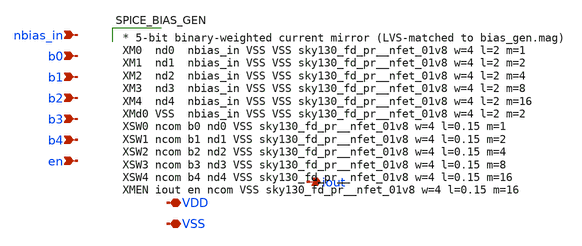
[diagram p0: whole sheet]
** sch_path: bvm_analog_tapeout/analog/bias_gen/xschem/bias_gen.sch
**.subckt bias_gen nbias_in b0 b1 b2 b3 b4 en iout VDD VSS
*.ipin nbias_in
*.ipin b0
*.ipin b1
*.ipin b2
*.ipin b3
*.ipin b4
*.ipin en
*.opin iout
*.iopin VDD
*.iopin VSS
**** begin user architecture code

* 5-bit binary-weighted current mirror (LVS-matched to bias_gen.mag)
XM0  nd0  nbias_in VSS VSS sky130_fd_pr__nfet_01v8 w=4 l=2 m=1
XM1  nd1  nbias_in VSS VSS sky130_fd_pr__nfet_01v8 w=4 l=2 m=2
XM2  nd2  nbias_in VSS VSS sky130_fd_pr__nfet_01v8 w=4 l=2 m=4
XM3  nd3  nbias_in VSS VSS sky130_fd_pr__nfet_01v8 w=4 l=2 m=8
XM4  nd4  nbias_in VSS VSS sky130_fd_pr__nfet_01v8 w=4 l=2 m=16
XMd0 VSS  nbias_in VSS VSS sky130_fd_pr__nfet_01v8 w=4 l=2 m=2
XSW0 ncom b0 nd0 VSS sky130_fd_pr__nfet_01v8 w=4 l=0.15 m=1
XSW1 ncom b1 nd1 VSS sky130_fd_pr__nfet_01v8 w=4 l=0.15 m=2
XSW2 ncom b2 nd2 VSS sky130_fd_pr__nfet_01v8 w=4 l=0.15 m=4
XSW3 ncom b3 nd3 VSS sky130_fd_pr__nfet_01v8 w=4 l=0.15 m=8
XSW4 ncom b4 nd4 VSS sky130_fd_pr__nfet_01v8 w=4 l=0.15 m=16
XMEN iout en ncom VSS sky130_fd_pr__nfet_01v8 w=4 l=0.15 m=16

**** end user architecture code
**.ends
.end
